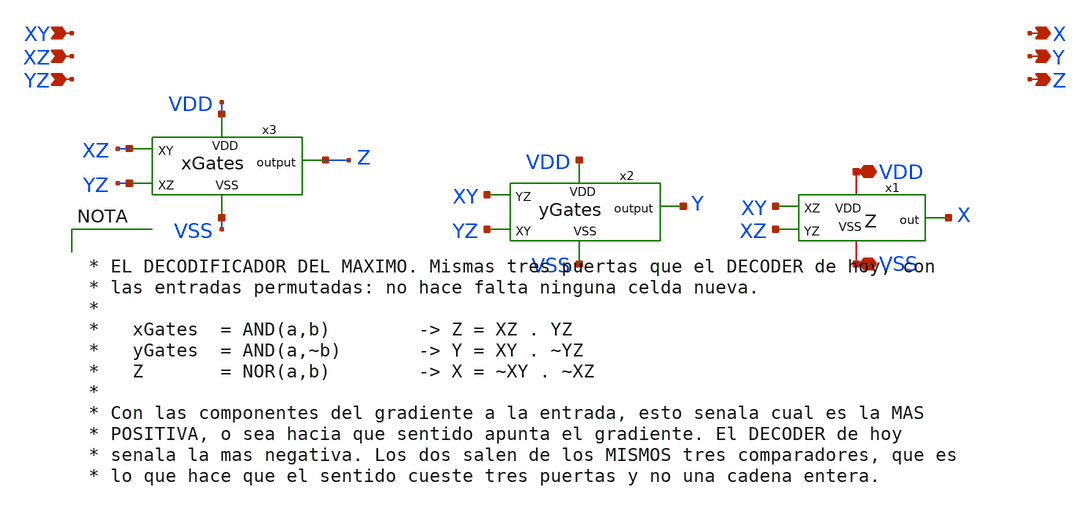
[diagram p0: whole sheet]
** sch_path: FINAL/XSCHEM_v2/DECODER_MAX.sch
**.subckt DECODER_MAX XY XZ YZ VDD VSS X Y Z
*.ipin XY
*.ipin XZ
*.ipin YZ
*.iopin VDD
*.iopin VSS
*.opin X
*.opin Y
*.opin Z
x3 VDD XZ Z YZ VSS xGates
x2 XY YZ VDD Y VSS yGates
x1 VSS VDD XY XZ X Z
**** begin user architecture code


* EL DECODIFICADOR DEL MAXIMO. Mismas tres puertas que el DECODER de hoy, con
* las entradas permutadas: no hace falta ninguna celda nueva.
*
*   xGates  = AND(a,b)        -> Z = XZ . YZ
*   yGates  = AND(a,~b)       -> Y = XY . ~YZ
*   Z       = NOR(a,b)        -> X = ~XY . ~XZ
*
* Con las componentes del gradiente a la entrada, esto senala cual es la MAS
* POSITIVA, o sea hacia que sentido apunta el gradiente. El DECODER de hoy
* senala la mas negativa. Los dos salen de los MISMOS tres comparadores, que es
* lo que hace que el sentido cueste tres puertas y no una cadena entera.


**** end user architecture code
**.ends
.end
